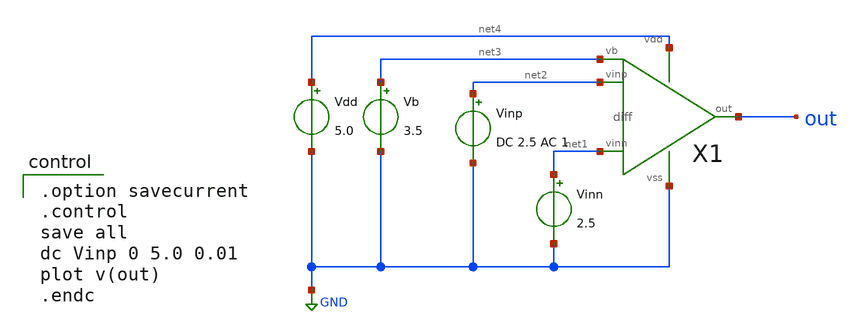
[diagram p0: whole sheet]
** sch_path: OR1/PTC06/opamp/diff_dc.sch
**.subckt diff_dc
Vdd net4 GND 5.0
Vb net3 GND 3.5
Vinn net1 GND 2.5
Vinp net2 GND DC 2.5 AC 1
X1 net2 net1 out net4 GND net3 diff
**** begin user architecture code

.option savecurrent
.control
save all
dc Vinp 0 5.0 0.01
plot v(out)
.endc

 .include $::LIB/mos.lib
.include $::LIB/passive.lib
.include $::LIB/diode.lib
**** end user architecture code
**.ends

* expanding   symbol:  diff.sym # of pins=6
** sym_path: diff.sym
** sch_path: diff.sch
.subckt diff vinp vinn out vdd vss vb
*.ipin vinn
*.ipin vinp
*.ipin vb
*.opin out
*.iopin vdd
*.iopin vss
M5 net2 vb vdd vdd pmos L=2u W=40u m=1
M1 net1 vinn net2 net2 pmos L=2u W=200u m=1
M2 out vinp net2 net2 pmos L=2u W=200u m=1
M3 net1 net1 vss vss nmos L=2u W=10u m=1
M4 out net1 vss vss nmos L=2u W=10u m=1
.ends

.GLOBAL GND
.end
